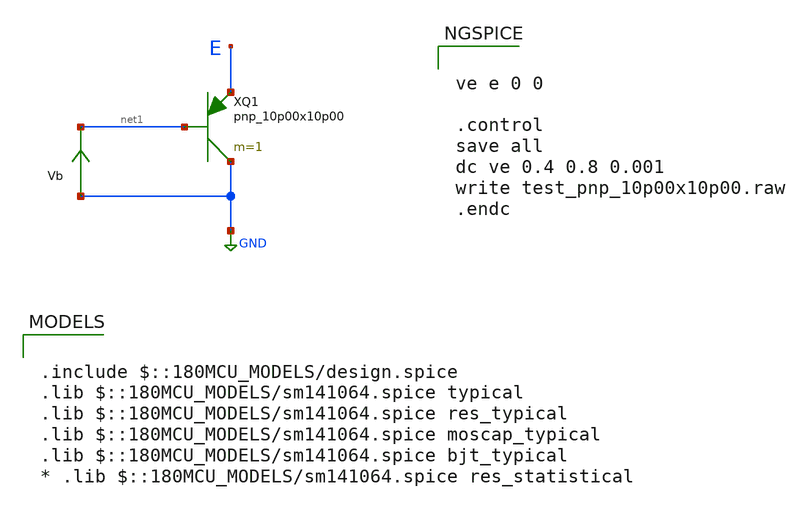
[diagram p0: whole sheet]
** sch_path: cells/xschem/tests/test_pnp_10p00x10p00.sch
* Copyright 2022 GlobalFoundries PDK Authors
* Licensed under the Apache License, Version 2.0 (the "License");
* you may not use this file except in compliance with the License.
* You may obtain a copy of the License at
* https://www.apache.org/licenses/LICENSE-2.0
* Unless required by applicable law or agreed to in writing, software
* distributed under the License is distributed on an "AS IS" BASIS,
* WITHOUT WARRANTIES OR CONDITIONS OF ANY KIND, either express or implied.
* See the License for the specific language governing permissions and
* limitations under the License.
**.subckt test_pnp_10p00x10p00
XQ1 GND net1 E pnp_10p00x10p00 m=1 par=1
Vb GND net1 0
.save i(vb)
**** begin user architecture code

.include $::180MCU_MODELS/design.spice
.lib $::180MCU_MODELS/sm141064.spice typical
.lib $::180MCU_MODELS/sm141064.spice res_typical
.lib $::180MCU_MODELS/sm141064.spice moscap_typical
.lib $::180MCU_MODELS/sm141064.spice bjt_typical
* .lib $::180MCU_MODELS/sm141064.spice res_statistical



ve e 0 0

.control
save all
dc ve 0.4 0.8 0.001
write test_pnp_10p00x10p00.raw
.endc


**** end user architecture code
**.ends
.GLOBAL GND
.end
